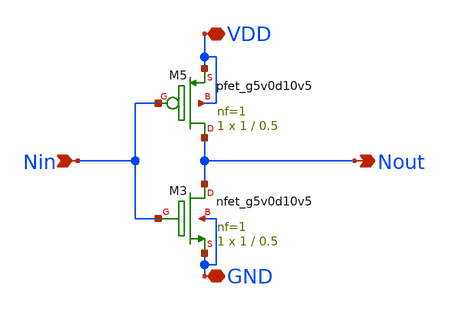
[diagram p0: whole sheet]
** sch_path: Analog Design Alan Rivera/Xschem/Sch/NOT.sch
**.subckt NOT Nin VDD GND Nout
*.ipin Nin
*.iopin VDD
*.iopin GND
*.opin Nout
XM3 Nout Nin GND GND sky130_fd_pr__nfet_g5v0d10v5 L=0.5 W=1 nf=1 ad='int((nf+1)/2) * W/nf * 0.29' as='int((nf+2)/2) * W/nf * 0.29'
+ pd='2*int((nf+1)/2) * (W/nf + 0.29)' ps='2*int((nf+2)/2) * (W/nf + 0.29)' nrd='0.29 / W' nrs='0.29 / W'
+ sa=0 sb=0 sd=0 mult=1 m=1
XM5 Nout Nin VDD VDD sky130_fd_pr__pfet_g5v0d10v5 L=0.5 W=1 nf=1 ad='int((nf+1)/2) * W/nf * 0.29' as='int((nf+2)/2) * W/nf * 0.29'
+ pd='2*int((nf+1)/2) * (W/nf + 0.29)' ps='2*int((nf+2)/2) * (W/nf + 0.29)' nrd='0.29 / W' nrs='0.29 / W'
+ sa=0 sb=0 sd=0 mult=1 m=1
**.ends
.end
